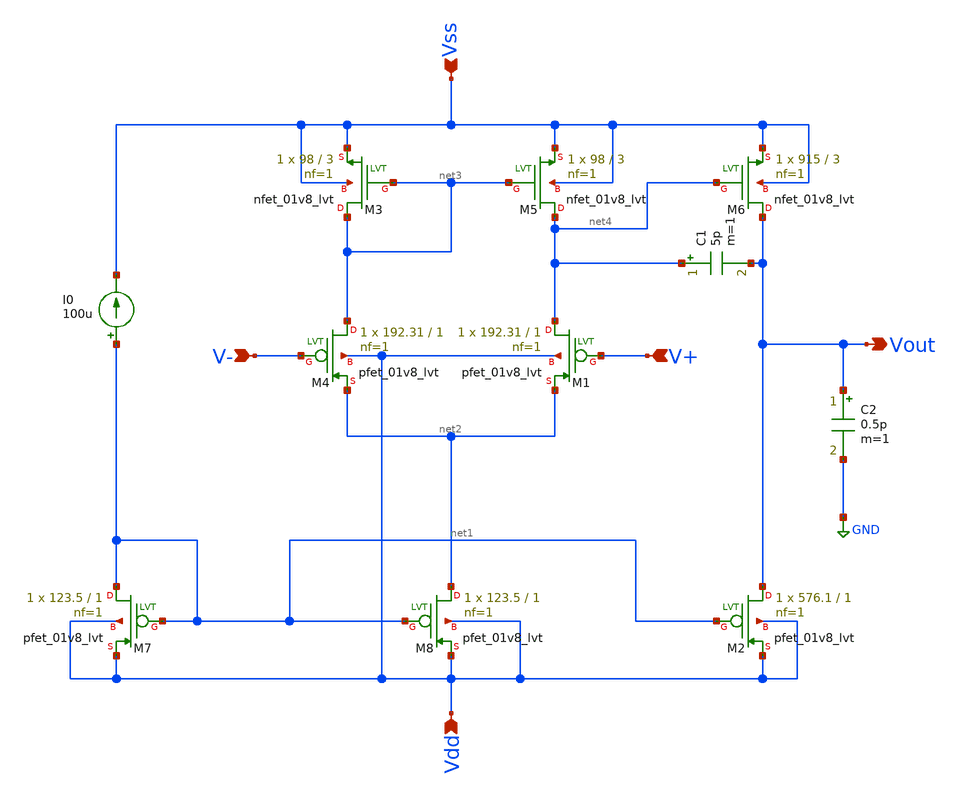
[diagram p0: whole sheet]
** sch_path: xschem/PMOS_OP_AMP.sch
**.subckt PMOS_OP_AMP Vout Vdd Vss V+ V-
*.opin Vout
*.ipin Vdd
*.ipin Vss
*.ipin V+
*.ipin V-
I0 net1 Vss 100u
C1 net4 Vout 5p m=1
C2 Vout GND 0.5p m=1
XM2 Vout net1 Vdd Vdd sky130_fd_pr__pfet_01v8_lvt L=1 W=576.1 nf=1 ad='int((1 + 1)/2) * 576.1 / 1 * 0.29'
+ as='int((1 + 2)/2) * 576.1 / 1 * 0.29' pd='2*int((1 + 1)/2) * (576.1 / 1 + 0.29)' ps='2*int((1 + 2)/2) * (576.1 / 1 + 0.29)'
+ nrd='0.29 / 576.1 ' nrs='0.29 / 576.1 ' sa=0 sb=0 sd=0 mult=1 m=1
XM7 net1 net1 Vdd Vdd sky130_fd_pr__pfet_01v8_lvt L=1 W=123.5 nf=1 ad='int((1 + 1)/2) * 123.5 / 1 * 0.29'
+ as='int((1 + 2)/2) * 123.5 / 1 * 0.29' pd='2*int((1 + 1)/2) * (123.5 / 1 + 0.29)' ps='2*int((1 + 2)/2) * (123.5 / 1 + 0.29)'
+ nrd='0.29 / 123.5 ' nrs='0.29 / 123.5 ' sa=0 sb=0 sd=0 mult=1 m=1
XM8 net2 net1 Vdd Vdd sky130_fd_pr__pfet_01v8_lvt L=1 W=123.5 nf=1 ad='int((1 + 1)/2) * 123.5 / 1 * 0.29'
+ as='int((1 + 2)/2) * 123.5 / 1 * 0.29' pd='2*int((1 + 1)/2) * (123.5 / 1 + 0.29)' ps='2*int((1 + 2)/2) * (123.5 / 1 + 0.29)'
+ nrd='0.29 / 123.5 ' nrs='0.29 / 123.5 ' sa=0 sb=0 sd=0 mult=1 m=1
XM4 net3 V- net2 Vdd sky130_fd_pr__pfet_01v8_lvt L=1 W=192.31 nf=1 ad='int((1 + 1)/2) * 192.31 / 1 * 0.29'
+ as='int((1 + 2)/2) * 192.31 / 1 * 0.29' pd='2*int((1 + 1)/2) * (192.31 / 1 + 0.29)' ps='2*int((1 + 2)/2) * (192.31 / 1 + 0.29)'
+ nrd='0.29 / 192.31 ' nrs='0.29 / 192.31 ' sa=0 sb=0 sd=0 mult=1 m=1
XM1 net4 V+ net2 Vdd sky130_fd_pr__pfet_01v8_lvt L=1 W=192.31 nf=1 ad='int((1 + 1)/2) * 192.31 / 1 * 0.29'
+ as='int((1 + 2)/2) * 192.31 / 1 * 0.29' pd='2*int((1 + 1)/2) * (192.31 / 1 + 0.29)' ps='2*int((1 + 2)/2) * (192.31 / 1 + 0.29)'
+ nrd='0.29 / 192.31 ' nrs='0.29 / 192.31 ' sa=0 sb=0 sd=0 mult=1 m=1
XM5 net4 net3 Vss Vss sky130_fd_pr__nfet_01v8_lvt L=3 W=98 nf=1 ad='int((1 + 1)/2) * 98 / 1 * 0.29' as='int((1 + 2)/2) * 98 / 1 * 0.29'
+ pd='2*int((1 + 1)/2) * (98 / 1 + 0.29)' ps='2*int((1 + 2)/2) * (98 / 1 + 0.29)' nrd='0.29 / 98 ' nrs='0.29 / 98 '
+ sa=0 sb=0 sd=0 mult=1 m=1
XM3 net3 net3 Vss Vss sky130_fd_pr__nfet_01v8_lvt L=3 W=98 nf=1 ad='int((1 + 1)/2) * 98 / 1 * 0.29' as='int((1 + 2)/2) * 98 / 1 * 0.29'
+ pd='2*int((1 + 1)/2) * (98 / 1 + 0.29)' ps='2*int((1 + 2)/2) * (98 / 1 + 0.29)' nrd='0.29 / 98 ' nrs='0.29 / 98 '
+ sa=0 sb=0 sd=0 mult=1 m=1
XM6 Vout net4 Vss Vss sky130_fd_pr__nfet_01v8_lvt L=3 W=915 nf=1 ad='int((1 + 1)/2) * 915 / 1 * 0.29'
+ as='int((1 + 2)/2) * 915 / 1 * 0.29' pd='2*int((1 + 1)/2) * (915 / 1 + 0.29)' ps='2*int((1 + 2)/2) * (915 / 1 + 0.29)'
+ nrd='0.29 / 915 ' nrs='0.29 / 915 ' sa=0 sb=0 sd=0 mult=1 m=1
**.ends
.GLOBAL GND
.end
